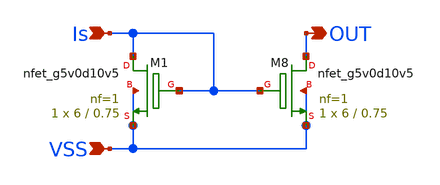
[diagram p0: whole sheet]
** sch_path: comparator_5v/mirror_bias.sch
**.subckt mirror_bias VSS Is OUT
*.ipin VSS
*.ipin Is
*.opin OUT
XM8 OUT Is VSS VSS sky130_fd_pr__nfet_g5v0d10v5 L=0.75 W=6 nf=1 ad='int((1 + 1)/2) * 6 / 1 * 0.29' as='int((1 + 2)/2) * 6 / 1 * 0.29'
+ pd='2*int((1 + 1)/2) * (6 / 1 + 0.29)' ps='2*int((1 + 2)/2) * (6 / 1 + 0.29)' nrd='0.29 / 6 ' nrs='0.29 / 6 '
+ sa=0 sb=0 sd=0 mult=1 m=1
XM1 Is Is VSS VSS sky130_fd_pr__nfet_g5v0d10v5 L=0.75 W=6 nf=1 ad='int((1 + 1)/2) * 6 / 1 * 0.29' as='int((1 + 2)/2) * 6 / 1 * 0.29'
+ pd='2*int((1 + 1)/2) * (6 / 1 + 0.29)' ps='2*int((1 + 2)/2) * (6 / 1 + 0.29)' nrd='0.29 / 6 ' nrs='0.29 / 6 '
+ sa=0 sb=0 sd=0 mult=1 m=1
**.ends
.end
